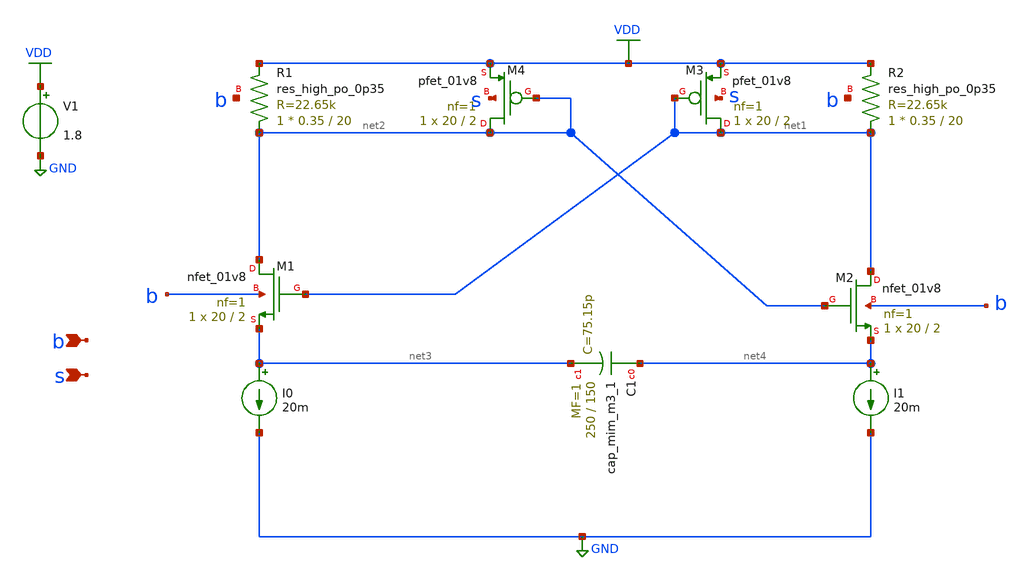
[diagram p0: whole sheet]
** sch_path: xschem/osc.sch
**.subckt osc b s
*.ipin b
*.ipin s
XM1 net2 net1 net3 b sky130_fd_pr__nfet_01v8 L=2 W=20 nf=1 ad='int((nf+1)/2) * W/nf * 0.29' as='int((nf+2)/2) * W/nf * 0.29'
+ pd='2*int((nf+1)/2) * (W/nf + 0.29)' ps='2*int((nf+2)/2) * (W/nf + 0.29)' nrd='0.29 / W' nrs='0.29 / W'
+ sa=0 sb=0 sd=0 mult=1 m=1
XM2 net1 net2 net4 b sky130_fd_pr__nfet_01v8 L=2 W=20 nf=1 ad='int((nf+1)/2) * W/nf * 0.29' as='int((nf+2)/2) * W/nf * 0.29'
+ pd='2*int((nf+1)/2) * (W/nf + 0.29)' ps='2*int((nf+2)/2) * (W/nf + 0.29)' nrd='0.29 / W' nrs='0.29 / W'
+ sa=0 sb=0 sd=0 mult=1 m=1
XM3 net1 net1 VDD s sky130_fd_pr__pfet_01v8 L=2 W=20 nf=1 ad='int((nf+1)/2) * W/nf * 0.29' as='int((nf+2)/2) * W/nf * 0.29'
+ pd='2*int((nf+1)/2) * (W/nf + 0.29)' ps='2*int((nf+2)/2) * (W/nf + 0.29)' nrd='0.29 / W' nrs='0.29 / W'
+ sa=0 sb=0 sd=0 mult=1 m=1
XM4 net2 net2 VDD s sky130_fd_pr__pfet_01v8 L=2 W=20 nf=1 ad='int((nf+1)/2) * W/nf * 0.29' as='int((nf+2)/2) * W/nf * 0.29'
+ pd='2*int((nf+1)/2) * (W/nf + 0.29)' ps='2*int((nf+2)/2) * (W/nf + 0.29)' nrd='0.29 / W' nrs='0.29 / W'
+ sa=0 sb=0 sd=0 mult=1 m=1
XR1 net2 VDD b sky130_fd_pr__res_high_po_0p35 L=20 mult=1 m=1
XR2 net1 VDD b sky130_fd_pr__res_high_po_0p35 L=20 mult=1 m=1
XC1 net4 net3 sky130_fd_pr__cap_mim_m3_1 W=250 L=150 MF=1 m=1
I0 net3 GND 20m
I1 net4 GND 20m
V1 VDD GND 1.8
**** begin user architecture code

** opencircuitdesign pdks install
.lib $::SKYWATER_MODELS/sky130.lib.spice tt




* .options filetype=ascii
.param mc_mm_switch=0
.param mc_pr_switch=0
.ic V(net1)=1.5 V(net2)=0
vs s 1.8 0
vb b 0 0
.control
tran 10p 100000p uic
write testbench.raw
quit 0
.endc
.end


**** end user architecture code
**.ends
.GLOBAL GND
.GLOBAL VDD
.end
